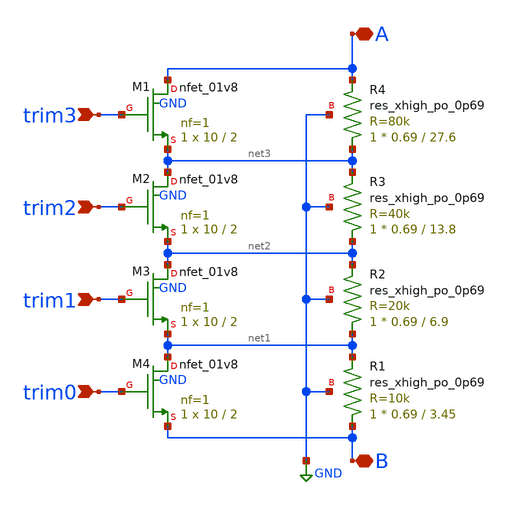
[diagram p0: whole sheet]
** sch_path: xschem/trim_res.sch
**.subckt trim_res trim0 trim1 trim2 trim3 B A
*.ipin trim0
*.ipin trim1
*.ipin trim2
*.ipin trim3
*.iopin B
*.iopin A
XM1 A trim3 net3 GND sky130_fd_pr__nfet_01v8 L=2 W=10 nf=1 ad='int((nf+1)/2) * W/nf * 0.29' as='int((nf+2)/2) * W/nf * 0.29'
+ pd='2*int((nf+1)/2) * (W/nf + 0.29)' ps='2*int((nf+2)/2) * (W/nf + 0.29)' nrd='0.29 / W' nrs='0.29 / W'
+ sa=0 sb=0 sd=0 mult=1 m=1
XM2 net3 trim2 net2 GND sky130_fd_pr__nfet_01v8 L=2 W=10 nf=1 ad='int((nf+1)/2) * W/nf * 0.29' as='int((nf+2)/2) * W/nf * 0.29'
+ pd='2*int((nf+1)/2) * (W/nf + 0.29)' ps='2*int((nf+2)/2) * (W/nf + 0.29)' nrd='0.29 / W' nrs='0.29 / W'
+ sa=0 sb=0 sd=0 mult=1 m=1
XM3 net2 trim1 net1 GND sky130_fd_pr__nfet_01v8 L=2 W=10 nf=1 ad='int((nf+1)/2) * W/nf * 0.29' as='int((nf+2)/2) * W/nf * 0.29'
+ pd='2*int((nf+1)/2) * (W/nf + 0.29)' ps='2*int((nf+2)/2) * (W/nf + 0.29)' nrd='0.29 / W' nrs='0.29 / W'
+ sa=0 sb=0 sd=0 mult=1 m=1
XM4 net1 trim0 B GND sky130_fd_pr__nfet_01v8 L=2 W=10 nf=1 ad='int((nf+1)/2) * W/nf * 0.29' as='int((nf+2)/2) * W/nf * 0.29'
+ pd='2*int((nf+1)/2) * (W/nf + 0.29)' ps='2*int((nf+2)/2) * (W/nf + 0.29)' nrd='0.29 / W' nrs='0.29 / W'
+ sa=0 sb=0 sd=0 mult=1 m=1
XR1 B net1 GND sky130_fd_pr__res_xhigh_po_0p69 L=3.45 mult=1 m=1
XR2 net1 net2 GND sky130_fd_pr__res_xhigh_po_0p69 L=6.9 mult=1 m=1
XR3 net2 net3 GND sky130_fd_pr__res_xhigh_po_0p69 L=13.8 mult=1 m=1
XR4 net3 A GND sky130_fd_pr__res_xhigh_po_0p69 L=27.6 mult=1 m=1
**.ends
.GLOBAL GND
.end
